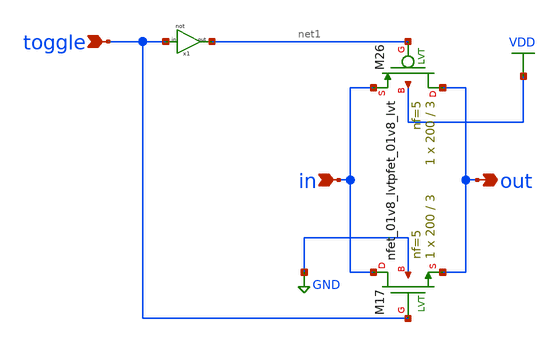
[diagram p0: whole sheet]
** sch_path: xschem/switch/switch.sch
**.subckt switch toggle in out
*.ipin toggle
*.ipin in
*.opin out
x1 net1 toggle not
XM26 out net1 in VDD sky130_fd_pr__pfet_01v8_lvt L=3 W=200 nf=5 ad='int((5 + 1)/2) * 200 / 5 * 0.29'
+ as='int((5 + 2)/2) * 200 / 5 * 0.29' pd='2*int((5 + 1)/2) * (200 / 5 + 0.29)' ps='2*int((5 + 2)/2) * (200 / 5 + 0.29)'
+ nrd='0.29 / 200 ' nrs='0.29 / 200 ' sa=0 sb=0 sd=0 mult=1 m=1
XM17 in toggle out GND sky130_fd_pr__nfet_01v8_lvt L=3 W=200 nf=5 ad='int((5 + 1)/2) * 200 / 5 * 0.29'
+ as='int((5 + 2)/2) * 200 / 5 * 0.29' pd='2*int((5 + 1)/2) * (200 / 5 + 0.29)' ps='2*int((5 + 2)/2) * (200 / 5 + 0.29)'
+ nrd='0.29 / 200 ' nrs='0.29 / 200 ' sa=0 sb=0 sd=0 mult=1 m=1
**.ends

* expanding   symbol:  not/not.sym # of pins=2
** sym_path: xschem/not/not.sym
** sch_path: xschem/not/not.sch
.subckt not out in
*.ipin in
*.opin out
XM10 out in VDD VDD sky130_fd_pr__pfet_01v8_lvt L=0.35 W=1 nf=1 ad='int((1 + 1)/2) * 1 / 1 * 0.29' as='int((1 + 2)/2) * 1 / 1 * 0.29'
+ pd='2*int((1 + 1)/2) * (1 / 1 + 0.29)' ps='2*int((1 + 2)/2) * (1 / 1 + 0.29)' nrd='0.29 / 1 ' nrs='0.29 / 1 '
+ sa=0 sb=0 sd=0 mult=1 m=1
XM1 out in GND GND sky130_fd_pr__nfet_01v8_lvt L=0.15 W=1 nf=1 ad='int((1 + 1)/2) * 1 / 1 * 0.29' as='int((1 + 2)/2) * 1 / 1 * 0.29'
+ pd='2*int((1 + 1)/2) * (1 / 1 + 0.29)' ps='2*int((1 + 2)/2) * (1 / 1 + 0.29)' nrd='0.29 / 1 ' nrs='0.29 / 1 '
+ sa=0 sb=0 sd=0 mult=1 m=1
.ends

.GLOBAL VDD
.GLOBAL GND
.end
